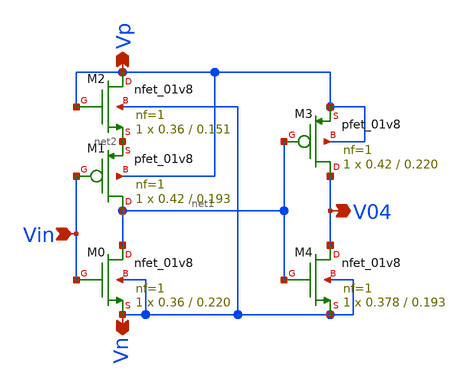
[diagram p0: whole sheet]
** sch_path: xschem/Vth_sch/Symbol/th04.sch
**.subckt th04 Vn Vp Vin V04
*.opin Vn
*.opin Vp
*.ipin Vin
*.opin V04
XM3 V04 net1 Vp Vp sky130_fd_pr__pfet_01v8 L=0.220 W=0.42 nf=1 ad='int((nf+1)/2) * W/nf * 0.29' as='int((nf+2)/2) * W/nf * 0.29'
+ pd='2*int((nf+1)/2) * (W/nf + 0.29)' ps='2*int((nf+2)/2) * (W/nf + 0.29)' nrd='0.29 / W' nrs='0.29 / W'
+ sa=0 sb=0 sd=0 mult=1 m=1
XM4 V04 net1 Vn Vn sky130_fd_pr__nfet_01v8 L=0.193 W=0.378 nf=1 ad='int((nf+1)/2) * W/nf * 0.29' as='int((nf+2)/2) * W/nf * 0.29'
+ pd='2*int((nf+1)/2) * (W/nf + 0.29)' ps='2*int((nf+2)/2) * (W/nf + 0.29)' nrd='0.29 / W' nrs='0.29 / W'
+ sa=0 sb=0 sd=0 mult=1 m=1
XM1 net1 Vin net2 Vp sky130_fd_pr__pfet_01v8 L=0.193 W=0.42 nf=1 ad='int((nf+1)/2) * W/nf * 0.29' as='int((nf+2)/2) * W/nf * 0.29'
+ pd='2*int((nf+1)/2) * (W/nf + 0.29)' ps='2*int((nf+2)/2) * (W/nf + 0.29)' nrd='0.29 / W' nrs='0.29 / W'
+ sa=0 sb=0 sd=0 mult=1 m=1
XM0 net1 Vin Vn Vn sky130_fd_pr__nfet_01v8 L=0.220 W=0.36 nf=1 ad='int((nf+1)/2) * W/nf * 0.29' as='int((nf+2)/2) * W/nf * 0.29'
+ pd='2*int((nf+1)/2) * (W/nf + 0.29)' ps='2*int((nf+2)/2) * (W/nf + 0.29)' nrd='0.29 / W' nrs='0.29 / W'
+ sa=0 sb=0 sd=0 mult=1 m=1
XM2 Vp Vp net2 Vn sky130_fd_pr__nfet_01v8 L=0.151 W=0.36 nf=1 ad='int((nf+1)/2) * W/nf * 0.29' as='int((nf+2)/2) * W/nf * 0.29'
+ pd='2*int((nf+1)/2) * (W/nf + 0.29)' ps='2*int((nf+2)/2) * (W/nf + 0.29)' nrd='0.29 / W' nrs='0.29 / W'
+ sa=0 sb=0 sd=0 mult=1 m=1
**.ends
.end
